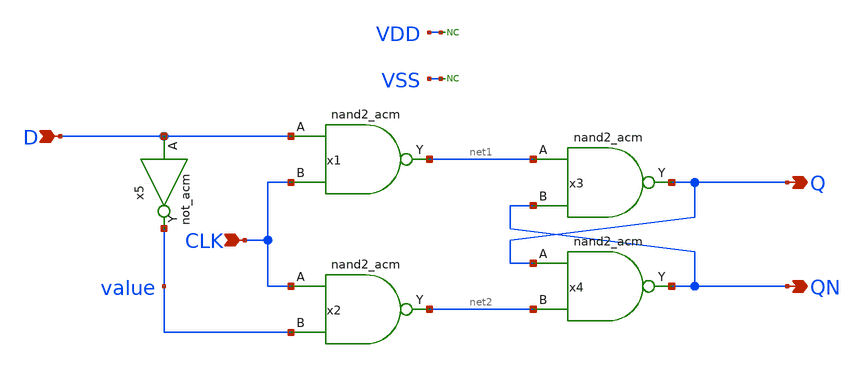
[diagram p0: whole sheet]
** sch_path: legacy/Examples/GF180MCU/xschem/symbol/DFF_acm.sch
**.subckt DFF_acm D CLK QN Q
*.ipin D
*.ipin CLK
*.opin QN
*.opin Q
x1 D CLK net1 VDD VSS nand2_acm
x2 CLK value net2 VDD VSS nand2_acm
x3 net1 QN Q VDD VSS nand2_acm
x4 Q net2 QN VDD VSS nand2_acm
x5 D value VDD VSS not_acm
* noconn VDD
* noconn VSS
**.ends
.end
